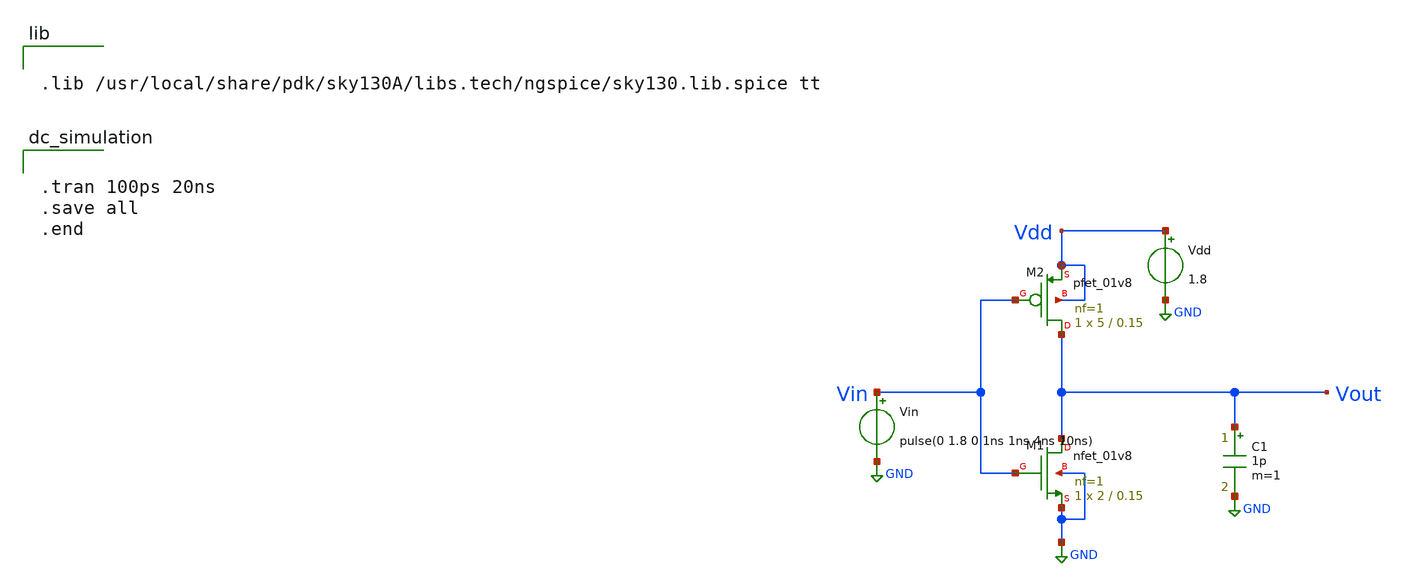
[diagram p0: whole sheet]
** sch_path: xschem/inverter.sch
**.subckt inverter
XM1 Vout Vin GND GND sky130_fd_pr__nfet_01v8 L=0.15 W=2 nf=1 ad='int((nf+1)/2) * W/nf * 0.29' as='int((nf+2)/2) * W/nf * 0.29'
+ pd='2*int((nf+1)/2) * (W/nf + 0.29)' ps='2*int((nf+2)/2) * (W/nf + 0.29)' nrd='0.29 / W' nrs='0.29 / W'
+ sa=0 sb=0 sd=0 mult=1 m=1
XM2 Vout Vin Vdd Vdd sky130_fd_pr__pfet_01v8 L=0.15 W=5 nf=1 ad='int((nf+1)/2) * W/nf * 0.29' as='int((nf+2)/2) * W/nf * 0.29'
+ pd='2*int((nf+1)/2) * (W/nf + 0.29)' ps='2*int((nf+2)/2) * (W/nf + 0.29)' nrd='0.29 / W' nrs='0.29 / W'
+ sa=0 sb=0 sd=0 mult=1 m=1
Vdd Vdd GND 1.8
Vin Vin GND pulse(0 1.8 0 1ns 1ns 4ns 10ns)
C1 Vout GND 1p m=1
**** begin user architecture code


.lib /usr/local/share/pdk/sky130A/libs.tech/ngspice/sky130.lib.spice tt




.tran 100ps 20ns
.save all
.end


**** end user architecture code
**.ends
.GLOBAL GND
.end
